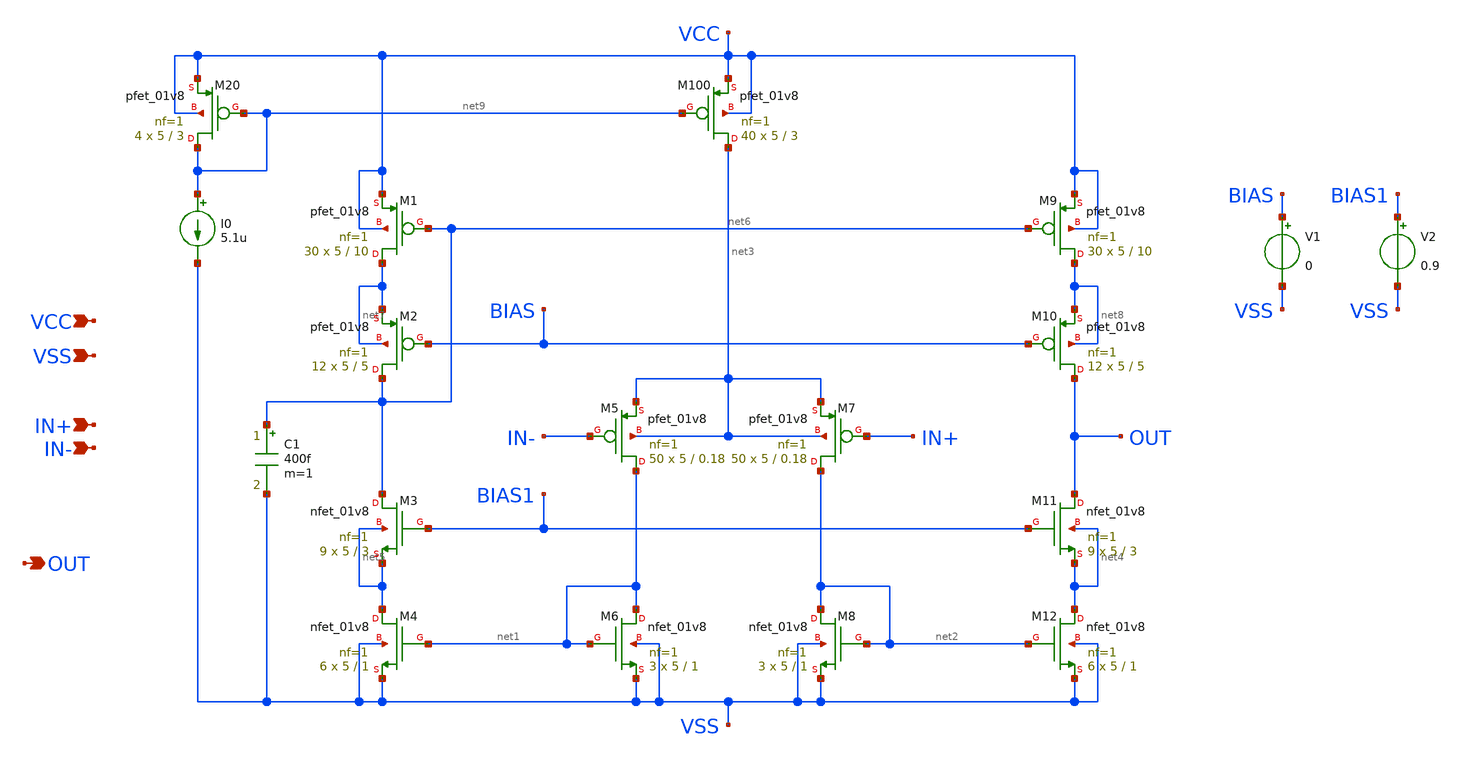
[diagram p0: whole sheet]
** sch_path: opamp_cascode.sch
**.subckt opamp_cascode IN+ IN- VCC VSS OUT
*.ipin IN+
*.ipin IN-
*.ipin VCC
*.ipin VSS
*.opin OUT
XM9 net8 net6 VCC VCC sky130_fd_pr__pfet_01v8 L=10 W=5 nf=1 ad='int((nf+1)/2) * W/nf * 0.29' as='int((nf+2)/2) * W/nf * 0.29'
+ pd='2*int((nf+1)/2) * (W/nf + 0.29)' ps='2*int((nf+2)/2) * (W/nf + 0.29)' nrd='0.29 / W' nrs='0.29 / W'
+ sa=0 sb=0 sd=0 mult=30 m=30
XM1 net7 net6 VCC VCC sky130_fd_pr__pfet_01v8 L=10 W=5 nf=1 ad='int((nf+1)/2) * W/nf * 0.29' as='int((nf+2)/2) * W/nf * 0.29'
+ pd='2*int((nf+1)/2) * (W/nf + 0.29)' ps='2*int((nf+2)/2) * (W/nf + 0.29)' nrd='0.29 / W' nrs='0.29 / W'
+ sa=0 sb=0 sd=0 mult=30 m=30
XM100 net3 net9 VCC VCC sky130_fd_pr__pfet_01v8 L=3 W=5 nf=1 ad='int((nf+1)/2) * W/nf * 0.29' as='int((nf+2)/2) * W/nf * 0.29'
+ pd='2*int((nf+1)/2) * (W/nf + 0.29)' ps='2*int((nf+2)/2) * (W/nf + 0.29)' nrd='0.29 / W' nrs='0.29 / W'
+ sa=0 sb=0 sd=0 mult=40 m=40
XM20 net9 net9 VCC VCC sky130_fd_pr__pfet_01v8 L=3 W=5 nf=1 ad='int((nf+1)/2) * W/nf * 0.29' as='int((nf+2)/2) * W/nf * 0.29'
+ pd='2*int((nf+1)/2) * (W/nf + 0.29)' ps='2*int((nf+2)/2) * (W/nf + 0.29)' nrd='0.29 / W' nrs='0.29 / W'
+ sa=0 sb=0 sd=0 mult=4 m=4
I0 net9 VSS 5.1u
XM10 OUT BIAS net8 net8 sky130_fd_pr__pfet_01v8 L=5 W=5 nf=1 ad='int((nf+1)/2) * W/nf * 0.29' as='int((nf+2)/2) * W/nf * 0.29'
+ pd='2*int((nf+1)/2) * (W/nf + 0.29)' ps='2*int((nf+2)/2) * (W/nf + 0.29)' nrd='0.29 / W' nrs='0.29 / W'
+ sa=0 sb=0 sd=0 mult=12 m=12
XM2 net6 BIAS net7 net7 sky130_fd_pr__pfet_01v8 L=5 W=5 nf=1 ad='int((nf+1)/2) * W/nf * 0.29' as='int((nf+2)/2) * W/nf * 0.29'
+ pd='2*int((nf+1)/2) * (W/nf + 0.29)' ps='2*int((nf+2)/2) * (W/nf + 0.29)' nrd='0.29 / W' nrs='0.29 / W'
+ sa=0 sb=0 sd=0 mult=12 m=12
XM5 net1 IN- net3 net3 sky130_fd_pr__pfet_01v8 L=0.18 W=5 nf=1 ad='int((nf+1)/2) * W/nf * 0.29' as='int((nf+2)/2) * W/nf * 0.29'
+ pd='2*int((nf+1)/2) * (W/nf + 0.29)' ps='2*int((nf+2)/2) * (W/nf + 0.29)' nrd='0.29 / W' nrs='0.29 / W'
+ sa=0 sb=0 sd=0 mult=50 m=50
XM7 net2 IN+ net3 net3 sky130_fd_pr__pfet_01v8 L=0.18 W=5 nf=1 ad='int((nf+1)/2) * W/nf * 0.29' as='int((nf+2)/2) * W/nf * 0.29'
+ pd='2*int((nf+1)/2) * (W/nf + 0.29)' ps='2*int((nf+2)/2) * (W/nf + 0.29)' nrd='0.29 / W' nrs='0.29 / W'
+ sa=0 sb=0 sd=0 mult=50 m=50
XM6 net1 net1 VSS VSS sky130_fd_pr__nfet_01v8 L=1 W=5 nf=1 ad='int((nf+1)/2) * W/nf * 0.29' as='int((nf+2)/2) * W/nf * 0.29'
+ pd='2*int((nf+1)/2) * (W/nf + 0.29)' ps='2*int((nf+2)/2) * (W/nf + 0.29)' nrd='0.29 / W' nrs='0.29 / W'
+ sa=0 sb=0 sd=0 mult=3 m=3
XM8 net2 net2 VSS VSS sky130_fd_pr__nfet_01v8 L=1 W=5 nf=1 ad='int((nf+1)/2) * W/nf * 0.29' as='int((nf+2)/2) * W/nf * 0.29'
+ pd='2*int((nf+1)/2) * (W/nf + 0.29)' ps='2*int((nf+2)/2) * (W/nf + 0.29)' nrd='0.29 / W' nrs='0.29 / W'
+ sa=0 sb=0 sd=0 mult=3 m=3
XM12 net4 net2 VSS VSS sky130_fd_pr__nfet_01v8 L=1 W=5 nf=1 ad='int((nf+1)/2) * W/nf * 0.29' as='int((nf+2)/2) * W/nf * 0.29'
+ pd='2*int((nf+1)/2) * (W/nf + 0.29)' ps='2*int((nf+2)/2) * (W/nf + 0.29)' nrd='0.29 / W' nrs='0.29 / W'
+ sa=0 sb=0 sd=0 mult=6 m=6
XM4 net5 net1 VSS VSS sky130_fd_pr__nfet_01v8 L=1 W=5 nf=1 ad='int((nf+1)/2) * W/nf * 0.29' as='int((nf+2)/2) * W/nf * 0.29'
+ pd='2*int((nf+1)/2) * (W/nf + 0.29)' ps='2*int((nf+2)/2) * (W/nf + 0.29)' nrd='0.29 / W' nrs='0.29 / W'
+ sa=0 sb=0 sd=0 mult=6 m=6
XM11 OUT BIAS1 net4 net4 sky130_fd_pr__nfet_01v8 L=3 W=5 nf=1 ad='int((nf+1)/2) * W/nf * 0.29' as='int((nf+2)/2) * W/nf * 0.29'
+ pd='2*int((nf+1)/2) * (W/nf + 0.29)' ps='2*int((nf+2)/2) * (W/nf + 0.29)' nrd='0.29 / W' nrs='0.29 / W'
+ sa=0 sb=0 sd=0 mult=9 m=9
XM3 net6 BIAS1 net5 net5 sky130_fd_pr__nfet_01v8 L=3 W=5 nf=1 ad='int((nf+1)/2) * W/nf * 0.29' as='int((nf+2)/2) * W/nf * 0.29'
+ pd='2*int((nf+1)/2) * (W/nf + 0.29)' ps='2*int((nf+2)/2) * (W/nf + 0.29)' nrd='0.29 / W' nrs='0.29 / W'
+ sa=0 sb=0 sd=0 mult=9 m=9
V1 BIAS VSS 0
V2 BIAS1 VSS 0.9
C1 net6 VSS 400f m=1
**.ends
.end
